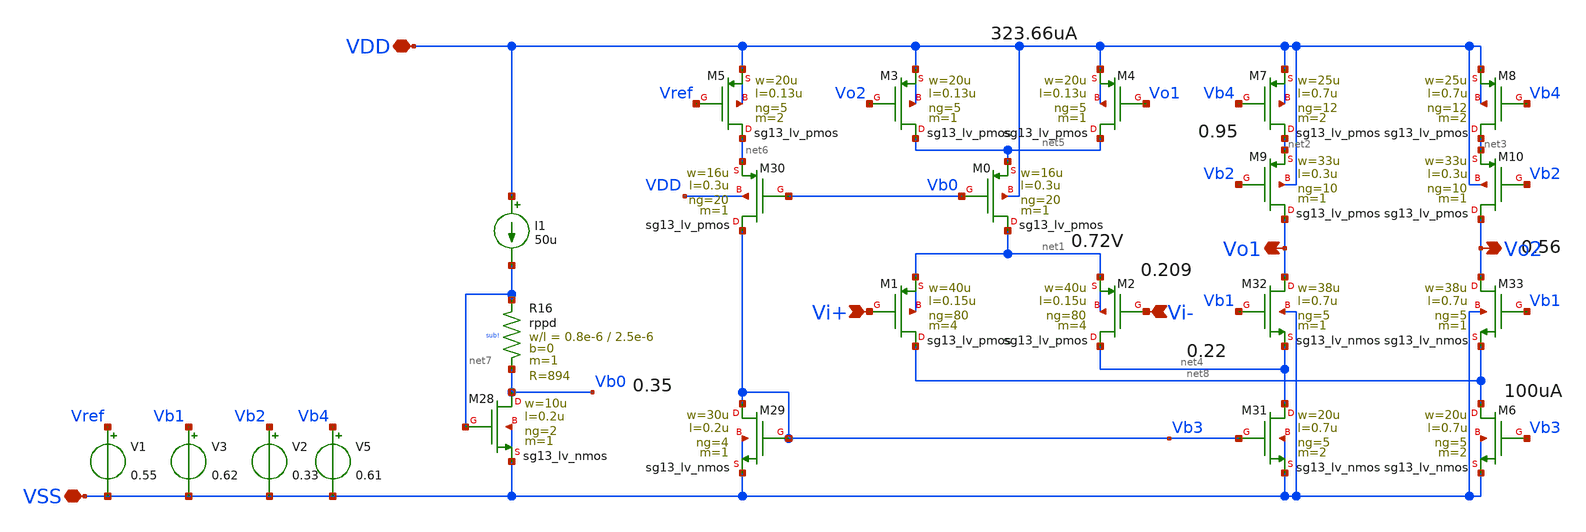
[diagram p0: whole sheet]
** sch_path: sch/blocks/gmBoosting.sch
**.subckt gmBoosting VDD VSS Vo1 Vo2 Vi+ Vi-
*.iopin VDD
*.iopin VSS
*.opin Vo1
*.opin Vo2
*.ipin Vi+
*.ipin Vi-
V3 Vb1 VSS 0.62
V2 Vb2 VSS 0.33
V5 Vb4 VSS 0.61
V1 Vref VSS 0.55
XM7 net2 Vb4 VDD VDD sg13_lv_pmos w=25u l=0.7u ng=12 m=2 mm_ok=1
XM1 net8 Vi+ net1 net1 sg13_lv_pmos w=40u l=0.15u ng=80 m=4 mm_ok=1
XM2 net4 Vi- net1 net1 sg13_lv_pmos w=40u l=0.15u ng=80 m=4 mm_ok=1
XM0 net1 Vb0 net5 VDD sg13_lv_pmos w=16u l=0.3u ng=20 m=1 mm_ok=1
XM6 net8 Vb3 VSS VSS sg13_lv_nmos w=20u l=0.7u ng=5 m=2 mm_ok=1
XM9 Vo1 Vb2 net2 VDD sg13_lv_pmos w=33u l=0.3u ng=10 m=1 mm_ok=1
XM10 Vo2 Vb2 net3 VDD sg13_lv_pmos w=33u l=0.3u ng=10 m=1 mm_ok=1
XM8 net3 Vb4 VDD VDD sg13_lv_pmos w=25u l=0.7u ng=12 m=2 mm_ok=1
XM3 net5 Vo2 VDD VDD sg13_lv_pmos w=20u l=0.13u ng=5 m=1 mm_ok=1
XM4 net5 Vo1 VDD VDD sg13_lv_pmos w=20u l=0.13u ng=5 m=1 mm_ok=1
XM5 net6 Vref VDD VDD sg13_lv_pmos w=20u l=0.13u ng=5 m=2 mm_ok=1
XM28 Vb0 net7 VSS VSS sg13_lv_nmos w=10u l=0.2u ng=2 m=1 mm_ok=1
XM29 Vb3 Vb3 VSS VSS sg13_lv_nmos w=30u l=0.2u ng=4 m=1 mm_ok=1
I1 VDD net7 50u
XR16 net7 Vb0 sub! rppd w=0.8e-6 l=2.5e-6 m=1 b=0 mm_ok=1
XM30 Vb3 Vb0 net6 VDD sg13_lv_pmos w=16u l=0.3u ng=20 m=1 mm_ok=1
XM31 net4 Vb3 VSS VSS sg13_lv_nmos w=20u l=0.7u ng=5 m=2 mm_ok=1
XM32 Vo1 Vb1 net4 VSS sg13_lv_nmos w=38u l=0.7u ng=5 m=1 mm_ok=1
XM33 Vo2 Vb1 net8 VSS sg13_lv_nmos w=38u l=0.7u ng=5 m=1 mm_ok=1
**.ends
.end
